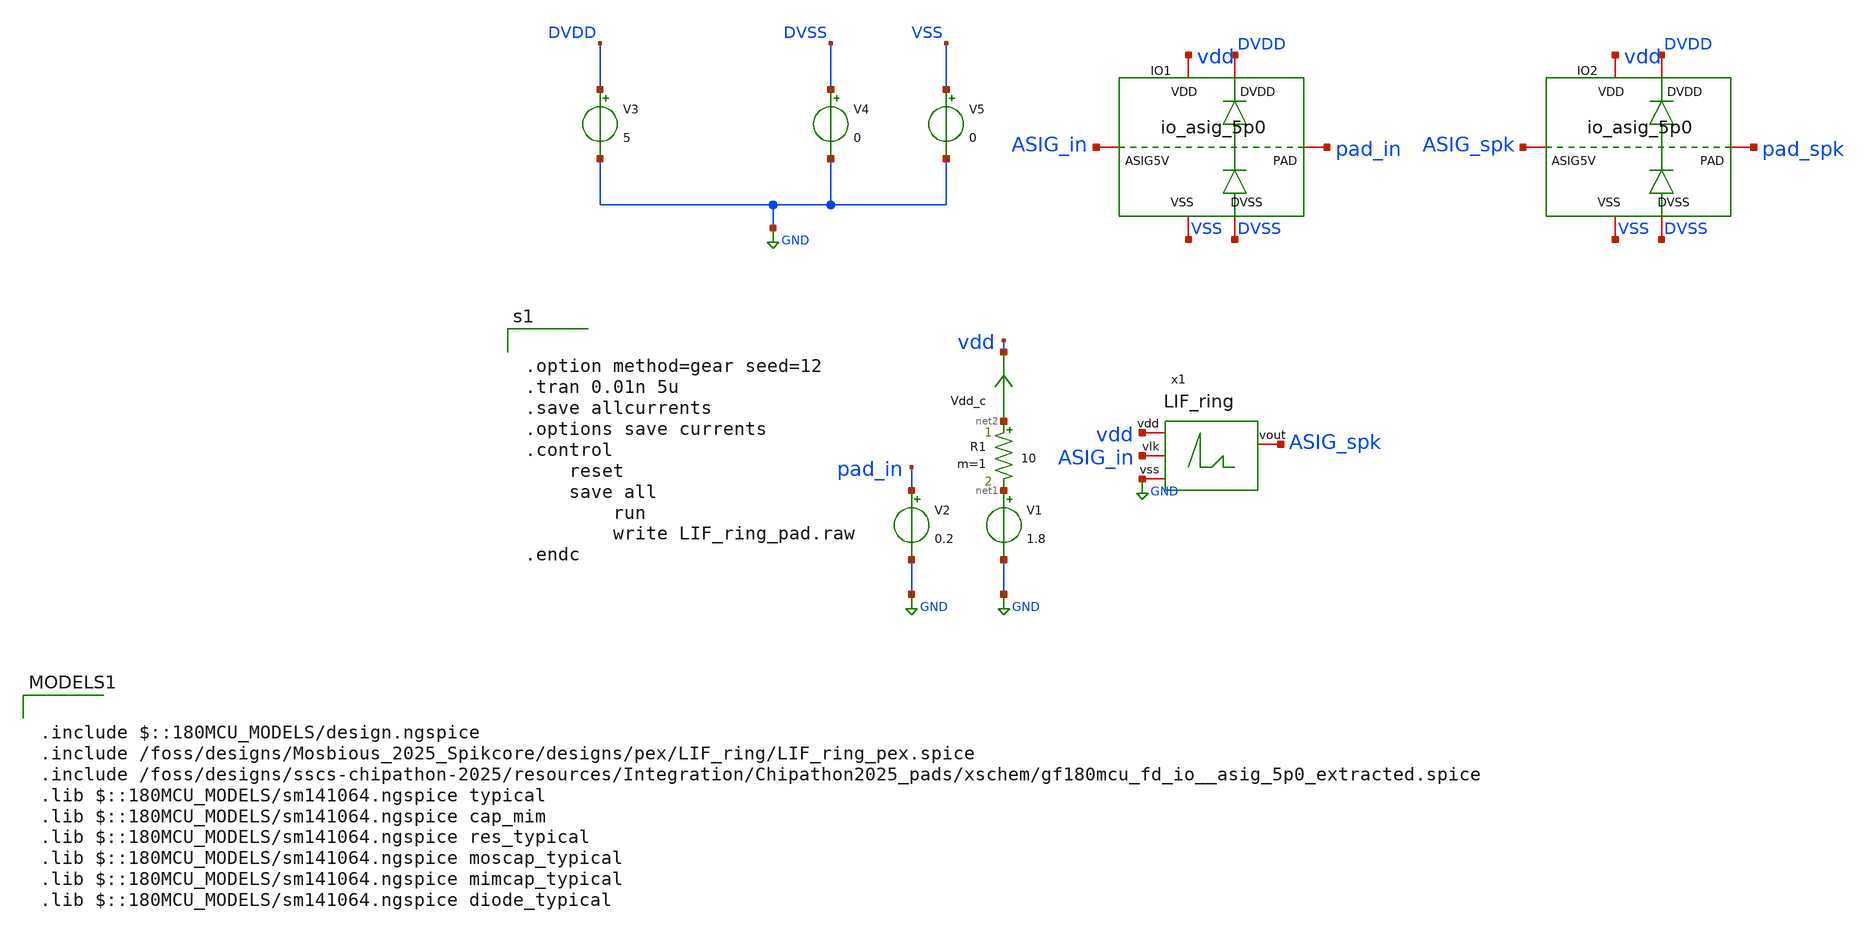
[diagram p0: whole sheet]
** sch_path: designs/pex_PADS/tb_LIF_ring/LIF_ring.sch
**.subckt LIF_ring
V1 net1 GND 1.8
Vdd_c net2 vdd 0
.save i(vdd_c)
R1 net2 net1 10 m=1
V2 pad_in GND 0.2
x1 vdd ASIG_in ASIG_spk GND LIF_ring
V3 DVDD GND 5
V4 DVSS GND 0
V5 VSS GND 0
XIO1 DVSS DVDD VSS vdd pad_in ASIG_in gf180mcu_fd_io__asig_5p0_extracted
XIO2 DVSS DVDD VSS vdd pad_spk ASIG_spk gf180mcu_fd_io__asig_5p0_extracted
**** begin user architecture code


.option method=gear seed=12
.tran 0.01n 5u
.save allcurrents
.options save currents
.control
	reset
	save all
        run
        write LIF_ring_pad.raw
.endc



.include $::180MCU_MODELS/design.ngspice
.include /foss/designs/Mosbious_2025_Spikcore/designs/pex/LIF_ring/LIF_ring_pex.spice
.include /foss/designs/sscs-chipathon-2025/resources/Integration/Chipathon2025_pads/xschem/gf180mcu_fd_io__asig_5p0_extracted.spice
.lib $::180MCU_MODELS/sm141064.ngspice typical
.lib $::180MCU_MODELS/sm141064.ngspice cap_mim
.lib $::180MCU_MODELS/sm141064.ngspice res_typical
.lib $::180MCU_MODELS/sm141064.ngspice moscap_typical
.lib $::180MCU_MODELS/sm141064.ngspice mimcap_typical
.lib $::180MCU_MODELS/sm141064.ngspice diode_typical

**** end user architecture code
**.ends
.GLOBAL GND
.end
